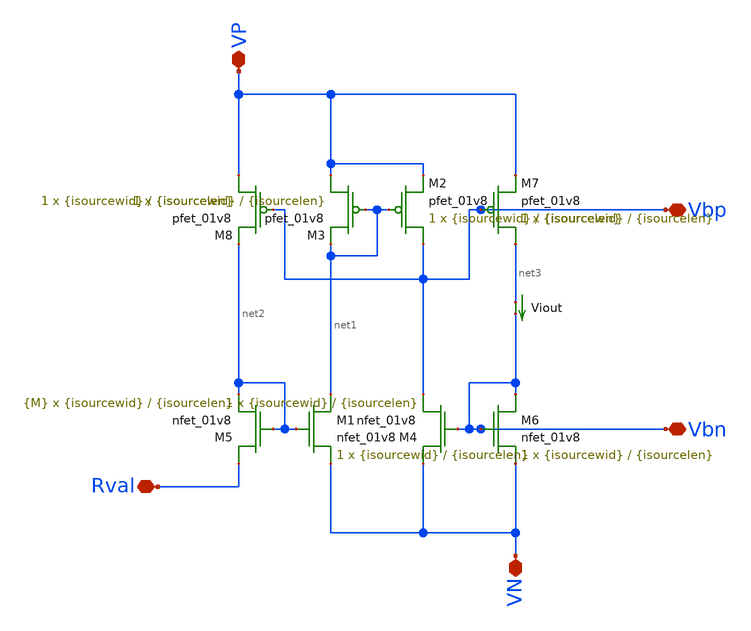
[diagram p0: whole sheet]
** sch_path: prelim-files/biasgen.sch
**.subckt biasgen Rval VN VP Vbp Vbn
*.iopin Rval
*.iopin VN
*.iopin VP
*.iopin Vbp
*.iopin Vbn
XM1 net1 net2 VN GND sky130_fd_pr__nfet_01v8 L={isourcelen} W={isourcewid} nf=1 ad='int((nf+1)/2) * W/nf * 0.29'
+ as='int((nf+2)/2) * W/nf * 0.29' pd='2*int((nf+1)/2) * (W/nf + 0.29)' ps='2*int((nf+2)/2) * (W/nf + 0.29)'
+ nrd='0.29 / W' nrs='0.29 / W' sa=0 sb=0 sd=0 mult=1 m=1
XM5 Rval net2 net2 GND sky130_fd_pr__nfet_01v8 L={isourcelen} W={isourcewid} nf=1 ad='int((nf+1)/2) * W/nf * 0.29'
+ as='int((nf+2)/2) * W/nf * 0.29' pd='2*int((nf+1)/2) * (W/nf + 0.29)' ps='2*int((nf+2)/2) * (W/nf + 0.29)'
+ nrd='0.29 / W' nrs='0.29 / W' sa=0 sb=0 sd=0 mult={M} m={M}
Viout net3 Vbn 0
.save i(viout)
XM8 VP Vbp net2 VDD sky130_fd_pr__pfet_01v8 L={isourcelen} W={isourcewid} nf=1 ad='int((nf+1)/2) * W/nf * 0.29'
+ as='int((nf+2)/2) * W/nf * 0.29' pd='2*int((nf+1)/2) * (W/nf + 0.29)' ps='2*int((nf+2)/2) * (W/nf + 0.29)'
+ nrd='0.29 / W' nrs='0.29 / W' sa=0 sb=0 sd=0 mult=1 m=1
XM3 VP net1 net1 VDD sky130_fd_pr__pfet_01v8 L={isourcelen} W={isourcewid} nf=1 ad='int((nf+1)/2) * W/nf * 0.29'
+ as='int((nf+2)/2) * W/nf * 0.29' pd='2*int((nf+1)/2) * (W/nf + 0.29)' ps='2*int((nf+2)/2) * (W/nf + 0.29)'
+ nrd='0.29 / W' nrs='0.29 / W' sa=0 sb=0 sd=0 mult=1 m=1
XM2 Vbp net1 VP VDD sky130_fd_pr__pfet_01v8 L={isourcelen} W={isourcewid} nf=1 ad='int((nf+1)/2) * W/nf * 0.29'
+ as='int((nf+2)/2) * W/nf * 0.29' pd='2*int((nf+1)/2) * (W/nf + 0.29)' ps='2*int((nf+2)/2) * (W/nf + 0.29)'
+ nrd='0.29 / W' nrs='0.29 / W' sa=0 sb=0 sd=0 mult=1 m=1
XM7 net3 Vbp VP VDD sky130_fd_pr__pfet_01v8 L={isourcelen} W={isourcewid} nf=1 ad='int((nf+1)/2) * W/nf * 0.29'
+ as='int((nf+2)/2) * W/nf * 0.29' pd='2*int((nf+1)/2) * (W/nf + 0.29)' ps='2*int((nf+2)/2) * (W/nf + 0.29)'
+ nrd='0.29 / W' nrs='0.29 / W' sa=0 sb=0 sd=0 mult=1 m=1
XM4 VN Vbn Vbp GND sky130_fd_pr__nfet_01v8 L={isourcelen} W={isourcewid} nf=1 ad='int((nf+1)/2) * W/nf * 0.29'
+ as='int((nf+2)/2) * W/nf * 0.29' pd='2*int((nf+1)/2) * (W/nf + 0.29)' ps='2*int((nf+2)/2) * (W/nf + 0.29)'
+ nrd='0.29 / W' nrs='0.29 / W' sa=0 sb=0 sd=0 mult=1 m=1
XM6 Vbn Vbn VN GND sky130_fd_pr__nfet_01v8 L={isourcelen} W={isourcewid} nf=1 ad='int((nf+1)/2) * W/nf * 0.29'
+ as='int((nf+2)/2) * W/nf * 0.29' pd='2*int((nf+1)/2) * (W/nf + 0.29)' ps='2*int((nf+2)/2) * (W/nf + 0.29)'
+ nrd='0.29 / W' nrs='0.29 / W' sa=0 sb=0 sd=0 mult=1 m=1
**.ends
.end
